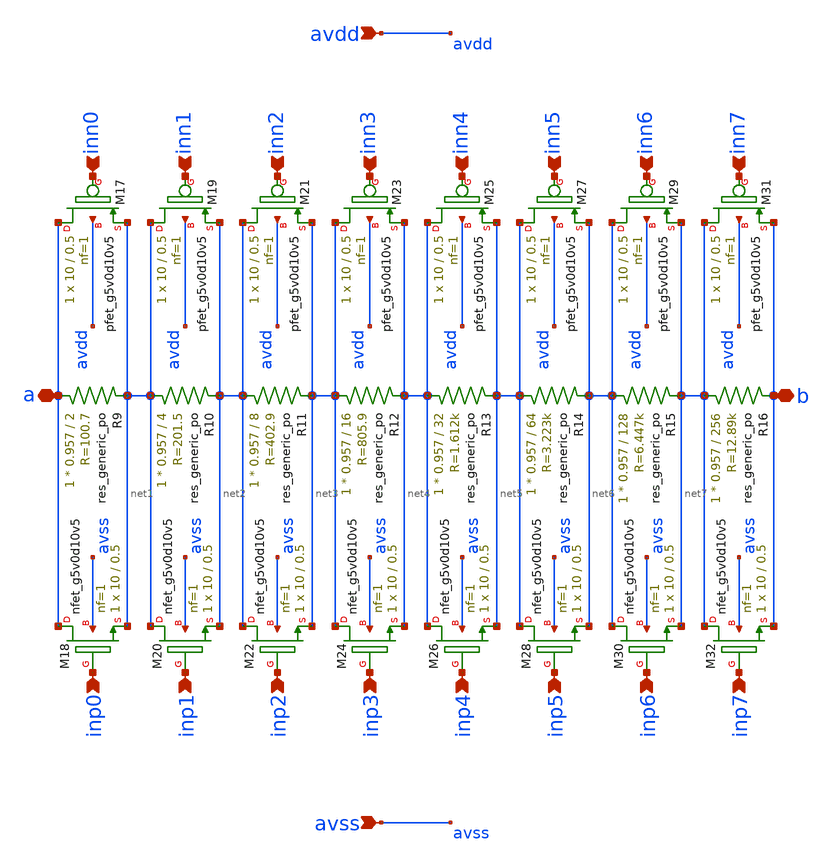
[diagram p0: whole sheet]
** sch_path: xschem/8bit_half_rheostat.sch
**.subckt 8bit_half_rheostat b a inn0 inn1 inn2 inn3 inn4 inn5 inn6 inn7 inp0 inp1 inp2 inp3 inp4
*+ inp5 inp6 inp7 avdd avss
*.iopin b
*.iopin a
*.ipin inn0
*.ipin inn1
*.ipin inn2
*.ipin inn3
*.ipin inn4
*.ipin inn5
*.ipin inn6
*.ipin inn7
*.ipin inp0
*.ipin inp1
*.ipin inp2
*.ipin inp3
*.ipin inp4
*.ipin inp5
*.ipin inp6
*.ipin inp7
*.ipin avdd
*.ipin avss
XM17 a inn0 net1 avdd sky130_fd_pr__pfet_g5v0d10v5 L=0.5 W=10 nf=1 ad='int((nf+1)/2) * W/nf * 0.29' as='int((nf+2)/2) * W/nf * 0.29'
+ pd='2*int((nf+1)/2) * (W/nf + 0.29)' ps='2*int((nf+2)/2) * (W/nf + 0.29)' nrd='0.29 / W' nrs='0.29 / W'
+ sa=0 sb=0 sd=0 mult=1 m=1
XM18 a inp0 net1 avss sky130_fd_pr__nfet_g5v0d10v5 L=0.5 W=10 nf=1 ad='int((nf+1)/2) * W/nf * 0.29' as='int((nf+2)/2) * W/nf * 0.29'
+ pd='2*int((nf+1)/2) * (W/nf + 0.29)' ps='2*int((nf+2)/2) * (W/nf + 0.29)' nrd='0.29 / W' nrs='0.29 / W'
+ sa=0 sb=0 sd=0 mult=1 m=1
XM19 net1 inn1 net2 avdd sky130_fd_pr__pfet_g5v0d10v5 L=0.5 W=10 nf=1 ad='int((nf+1)/2) * W/nf * 0.29'
+ as='int((nf+2)/2) * W/nf * 0.29' pd='2*int((nf+1)/2) * (W/nf + 0.29)' ps='2*int((nf+2)/2) * (W/nf + 0.29)'
+ nrd='0.29 / W' nrs='0.29 / W' sa=0 sb=0 sd=0 mult=1 m=1
XM20 net1 inp1 net2 avss sky130_fd_pr__nfet_g5v0d10v5 L=0.5 W=10 nf=1 ad='int((nf+1)/2) * W/nf * 0.29'
+ as='int((nf+2)/2) * W/nf * 0.29' pd='2*int((nf+1)/2) * (W/nf + 0.29)' ps='2*int((nf+2)/2) * (W/nf + 0.29)'
+ nrd='0.29 / W' nrs='0.29 / W' sa=0 sb=0 sd=0 mult=1 m=1
XM21 net2 inn2 net3 avdd sky130_fd_pr__pfet_g5v0d10v5 L=0.5 W=10 nf=1 ad='int((nf+1)/2) * W/nf * 0.29'
+ as='int((nf+2)/2) * W/nf * 0.29' pd='2*int((nf+1)/2) * (W/nf + 0.29)' ps='2*int((nf+2)/2) * (W/nf + 0.29)'
+ nrd='0.29 / W' nrs='0.29 / W' sa=0 sb=0 sd=0 mult=1 m=1
XM22 net2 inp2 net3 avss sky130_fd_pr__nfet_g5v0d10v5 L=0.5 W=10 nf=1 ad='int((nf+1)/2) * W/nf * 0.29'
+ as='int((nf+2)/2) * W/nf * 0.29' pd='2*int((nf+1)/2) * (W/nf + 0.29)' ps='2*int((nf+2)/2) * (W/nf + 0.29)'
+ nrd='0.29 / W' nrs='0.29 / W' sa=0 sb=0 sd=0 mult=1 m=1
XM23 net3 inn3 net4 avdd sky130_fd_pr__pfet_g5v0d10v5 L=0.5 W=10 nf=1 ad='int((nf+1)/2) * W/nf * 0.29'
+ as='int((nf+2)/2) * W/nf * 0.29' pd='2*int((nf+1)/2) * (W/nf + 0.29)' ps='2*int((nf+2)/2) * (W/nf + 0.29)'
+ nrd='0.29 / W' nrs='0.29 / W' sa=0 sb=0 sd=0 mult=1 m=1
XM24 net3 inp3 net4 avss sky130_fd_pr__nfet_g5v0d10v5 L=0.5 W=10 nf=1 ad='int((nf+1)/2) * W/nf * 0.29'
+ as='int((nf+2)/2) * W/nf * 0.29' pd='2*int((nf+1)/2) * (W/nf + 0.29)' ps='2*int((nf+2)/2) * (W/nf + 0.29)'
+ nrd='0.29 / W' nrs='0.29 / W' sa=0 sb=0 sd=0 mult=1 m=1
XM25 net4 inn4 net5 avdd sky130_fd_pr__pfet_g5v0d10v5 L=0.5 W=10 nf=1 ad='int((nf+1)/2) * W/nf * 0.29'
+ as='int((nf+2)/2) * W/nf * 0.29' pd='2*int((nf+1)/2) * (W/nf + 0.29)' ps='2*int((nf+2)/2) * (W/nf + 0.29)'
+ nrd='0.29 / W' nrs='0.29 / W' sa=0 sb=0 sd=0 mult=1 m=1
XM26 net4 inp4 net5 avss sky130_fd_pr__nfet_g5v0d10v5 L=0.5 W=10 nf=1 ad='int((nf+1)/2) * W/nf * 0.29'
+ as='int((nf+2)/2) * W/nf * 0.29' pd='2*int((nf+1)/2) * (W/nf + 0.29)' ps='2*int((nf+2)/2) * (W/nf + 0.29)'
+ nrd='0.29 / W' nrs='0.29 / W' sa=0 sb=0 sd=0 mult=1 m=1
XM27 net5 inn5 net6 avdd sky130_fd_pr__pfet_g5v0d10v5 L=0.5 W=10 nf=1 ad='int((nf+1)/2) * W/nf * 0.29'
+ as='int((nf+2)/2) * W/nf * 0.29' pd='2*int((nf+1)/2) * (W/nf + 0.29)' ps='2*int((nf+2)/2) * (W/nf + 0.29)'
+ nrd='0.29 / W' nrs='0.29 / W' sa=0 sb=0 sd=0 mult=1 m=1
XM28 net5 inp5 net6 avss sky130_fd_pr__nfet_g5v0d10v5 L=0.5 W=10 nf=1 ad='int((nf+1)/2) * W/nf * 0.29'
+ as='int((nf+2)/2) * W/nf * 0.29' pd='2*int((nf+1)/2) * (W/nf + 0.29)' ps='2*int((nf+2)/2) * (W/nf + 0.29)'
+ nrd='0.29 / W' nrs='0.29 / W' sa=0 sb=0 sd=0 mult=1 m=1
XM29 net6 inn6 net7 avdd sky130_fd_pr__pfet_g5v0d10v5 L=0.5 W=10 nf=1 ad='int((nf+1)/2) * W/nf * 0.29'
+ as='int((nf+2)/2) * W/nf * 0.29' pd='2*int((nf+1)/2) * (W/nf + 0.29)' ps='2*int((nf+2)/2) * (W/nf + 0.29)'
+ nrd='0.29 / W' nrs='0.29 / W' sa=0 sb=0 sd=0 mult=1 m=1
XM30 net6 inp6 net7 avss sky130_fd_pr__nfet_g5v0d10v5 L=0.5 W=10 nf=1 ad='int((nf+1)/2) * W/nf * 0.29'
+ as='int((nf+2)/2) * W/nf * 0.29' pd='2*int((nf+1)/2) * (W/nf + 0.29)' ps='2*int((nf+2)/2) * (W/nf + 0.29)'
+ nrd='0.29 / W' nrs='0.29 / W' sa=0 sb=0 sd=0 mult=1 m=1
XM31 net7 inn7 b avdd sky130_fd_pr__pfet_g5v0d10v5 L=0.5 W=10 nf=1 ad='int((nf+1)/2) * W/nf * 0.29' as='int((nf+2)/2) * W/nf * 0.29'
+ pd='2*int((nf+1)/2) * (W/nf + 0.29)' ps='2*int((nf+2)/2) * (W/nf + 0.29)' nrd='0.29 / W' nrs='0.29 / W'
+ sa=0 sb=0 sd=0 mult=1 m=1
XM32 net7 inp7 b avss sky130_fd_pr__nfet_g5v0d10v5 L=0.5 W=10 nf=1 ad='int((nf+1)/2) * W/nf * 0.29' as='int((nf+2)/2) * W/nf * 0.29'
+ pd='2*int((nf+1)/2) * (W/nf + 0.29)' ps='2*int((nf+2)/2) * (W/nf + 0.29)' nrd='0.29 / W' nrs='0.29 / W'
+ sa=0 sb=0 sd=0 mult=1 m=1
XR9 a net1 sky130_fd_pr__res_generic_po W=0.957 L=2 m=1
XR10 net1 net2 sky130_fd_pr__res_generic_po W=0.957 L=4 m=1
XR11 net2 net3 sky130_fd_pr__res_generic_po W=0.957 L=8 m=1
XR12 net3 net4 sky130_fd_pr__res_generic_po W=0.957 L=16 m=1
XR13 net4 net5 sky130_fd_pr__res_generic_po W=0.957 L=32 m=1
XR14 net5 net6 sky130_fd_pr__res_generic_po W=0.957 L=64 m=1
XR15 net6 net7 sky130_fd_pr__res_generic_po W=0.957 L=128 m=1
XR16 net7 b sky130_fd_pr__res_generic_po W=0.957 L=256 m=1
**.ends
.end
